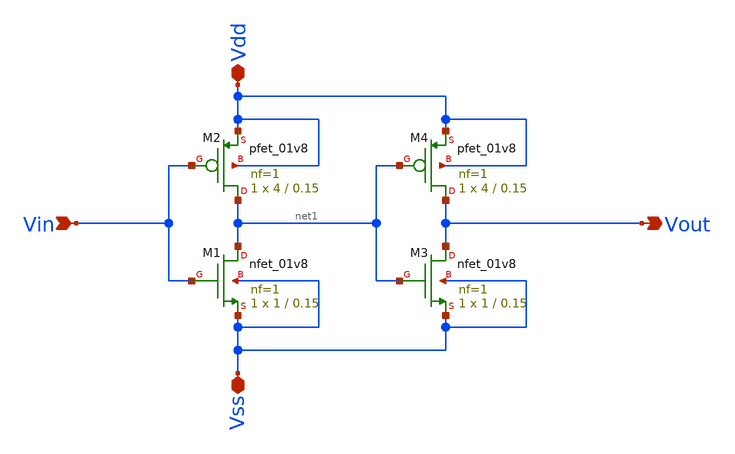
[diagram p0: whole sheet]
** sch_path: Current Starved VCO for PLL/xschem/buffer.sch
**.subckt buffer Vout Vin Vss Vdd
*.opin Vout
*.ipin Vin
*.iopin Vss
*.iopin Vdd
XM2 net1 Vin Vdd Vdd sky130_fd_pr__pfet_01v8 L=0.15 W=4 nf=1 ad='int((nf+1)/2) * W/nf * 0.29' as='int((nf+2)/2) * W/nf * 0.29'
+ pd='2*int((nf+1)/2) * (W/nf + 0.29)' ps='2*int((nf+2)/2) * (W/nf + 0.29)' nrd='0.29 / W' nrs='0.29 / W'
+ sa=0 sb=0 sd=0 mult=1 m=1
XM4 Vout net1 Vdd Vdd sky130_fd_pr__pfet_01v8 L=0.15 W=4 nf=1 ad='int((nf+1)/2) * W/nf * 0.29' as='int((nf+2)/2) * W/nf * 0.29'
+ pd='2*int((nf+1)/2) * (W/nf + 0.29)' ps='2*int((nf+2)/2) * (W/nf + 0.29)' nrd='0.29 / W' nrs='0.29 / W'
+ sa=0 sb=0 sd=0 mult=1 m=1
XM1 net1 Vin Vss Vss sky130_fd_pr__nfet_01v8 L=0.15 W=1 nf=1 ad='int((nf+1)/2) * W/nf * 0.29' as='int((nf+2)/2) * W/nf * 0.29'
+ pd='2*int((nf+1)/2) * (W/nf + 0.29)' ps='2*int((nf+2)/2) * (W/nf + 0.29)' nrd='0.29 / W' nrs='0.29 / W'
+ sa=0 sb=0 sd=0 mult=1 m=1
XM3 Vout net1 Vss Vss sky130_fd_pr__nfet_01v8 L=0.15 W=1 nf=1 ad='int((nf+1)/2) * W/nf * 0.29' as='int((nf+2)/2) * W/nf * 0.29'
+ pd='2*int((nf+1)/2) * (W/nf + 0.29)' ps='2*int((nf+2)/2) * (W/nf + 0.29)' nrd='0.29 / W' nrs='0.29 / W'
+ sa=0 sb=0 sd=0 mult=1 m=1
**.ends
.end
